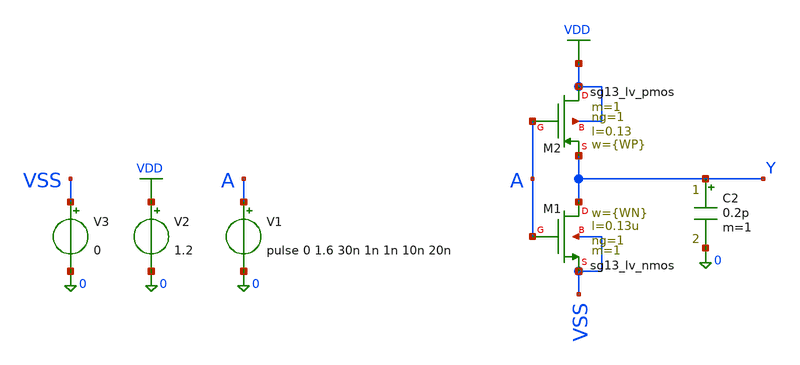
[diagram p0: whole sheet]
** sch_path: TSENSE8490-main/schematic/xschem/lvs-view/analog/inverter/testbench/inverter-tb.sch
**.subckt inverter-tb
V1 A 0 pulse 0 1.6 30n 1n 1n 10n 20n
V2 VDD 0 1.2
V3 VSS 0 0
C2 Y 0 0.2p m=1
XM1 Y A VSS VSS sg13_lv_nmos w={WN} l=0.13u ng=1 m=1 mm_ok=1
XM2 VDD A Y VDD sg13_lv_pmos w={WP} l=0.13 ng=1 m=1 mm_ok=1
**** begin user architecture code


.param temp=27
.param WP=1.12u WN=0.74u
.control

tran 0.2n 100n

write inverter-tb.raw a y
.endc





.lib cornerMOSlv.lib mos_tt
.lib cornerMOShv.lib mos_tt
.lib cornerRES.lib res_typ
.lib cornerDIO.lib dio_tt





.param temp=27
.param WN=1u WP=1u
.control
set wr_vecnames
set wr_onespace
*set wr_singlescale

* create one persistent plot for all sweep results
setplot new
set scratch = $curplot

* sweep value lists
compose wn_list values 0.5u 1u 2u 4u
compose wp_list values 1u 2u 4u 8u

let nwp = length(wp_list)
let nwn = length(wn_list)
let nruns = nwn * nwp
let nlast = nruns - 1

* flattened table columns
compose run start=0 stop=$&nlast step=1
let wp_vec   = vector(length(run))
let wn_vec   = vector(length(run))
let tplh_vec = vector(length(run))
let tphl_vec = vector(length(run))

let iwn = 0
let k   = 0

while iwn < nwn
  let iwp = 0

  while iwp < nwp
    * current sweep values
    let wp_now = wp_list[iwp]
    let wn_now = wn_list[iwn]

    alterparam WP = $&wp_now
    alterparam WN = $&wn_now
    reset

    tran 0.2n 100n

    meas tran tplh trig v(a) val=0.8 td=20n rise=1
    +              targ v(y) val=0.8 td=20n rise=1

    meas tran tphl trig v(a) val=0.8 td=20n fall=1
    +              targ v(y) val=0.8 td=20n fall=1

    * remember current tran plot
    set dt = $curplot

    * go back to scratch plot and store one row
    setplot $scratch
    let wp_vec[k]   = wp_now
    let wn_vec[k]   = wn_now
    let tplh_vec[k] = {$dt}.tplh
    let tphl_vec[k] = {$dt}.tphl

    let k   = k + 1
    let iwp = iwp + 1
  end

  let iwn = iwn + 1
end

*wrdata inverter-tb-meas.tbl run wp_vec wn_vec tplh_vec tphl_vec
write inverter-tb-meas.raw run wp_vec wn_vec tplh_vec tphl_vec
*print wp_vec wn_vec tplh_vec tphl_vec > inverter-tb-meas.txt
.endc


**** end user architecture code
**.ends
.GLOBAL VDD
.end
